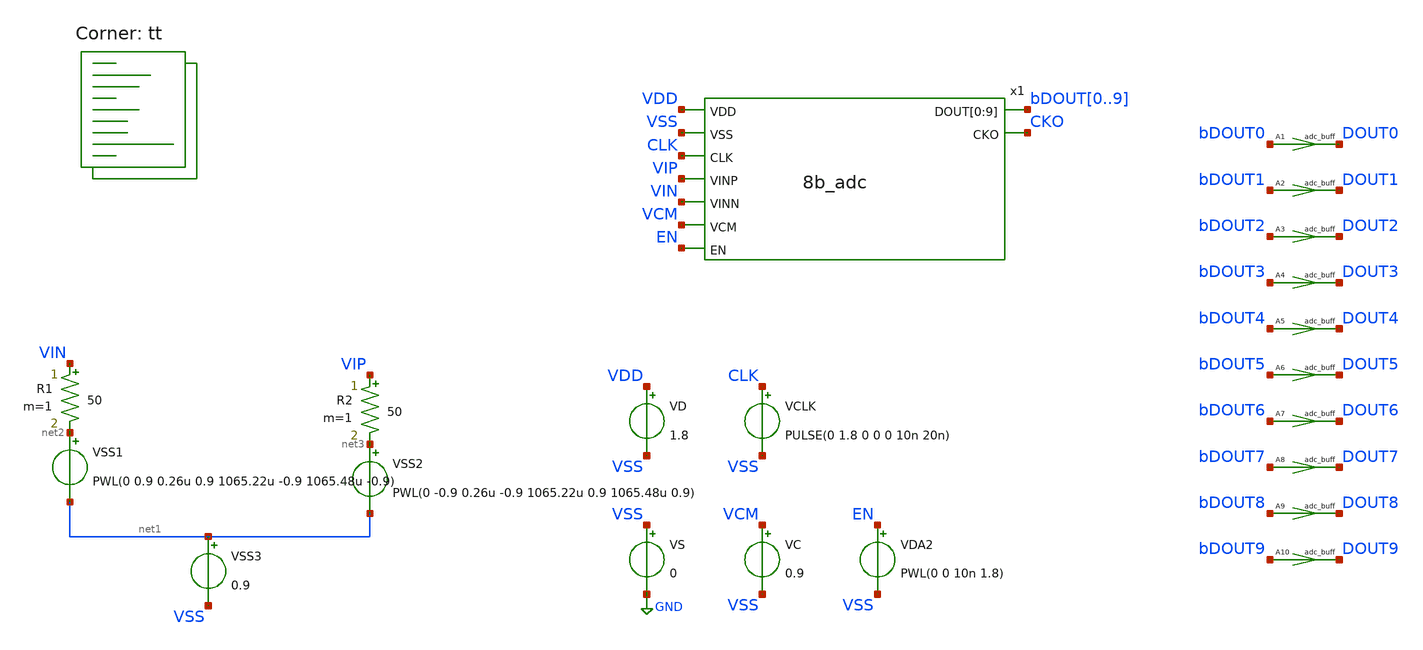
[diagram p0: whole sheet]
** sch_path: xschem/adc_tb_static.sch
**.subckt adc_tb_static
VSS1 net2 net1 PWL(0 0.9 0.26u 0.9 1065.22u -0.9 1065.48u -0.9)
VSS2 net3 net1 PWL(0 -0.9 0.26u -0.9 1065.22u 0.9 1065.48u 0.9)
VSS3 net1 VSS 0.9
R1 VIN net2 50 m=1
R2 VIP net3 50 m=1
VS VSS GND 0
VD VDD VSS 1.8
VCLK CLK VSS PULSE(0 1.8 0 0 0 10n 20n)
x1 VDD VSS CLK VIP VIN VCM EN bDOUT0 bDOUT1 bDOUT2 bDOUT3 bDOUT4 bDOUT5 bDOUT6 bDOUT7 bDOUT8 bDOUT9
+ CKO 8b_adc
VC VCM VSS 0.9
VDA2 EN VSS PWL(0 0 10n 1.8)
A1 [ bDOUT0 ] [ DOUT0 ] adc_buff
A2 [ bDOUT1 ] [ DOUT1 ] adc_buff
A3 [ bDOUT2 ] [ DOUT2 ] adc_buff
A4 [ bDOUT3 ] [ DOUT3 ] adc_buff
A5 [ bDOUT4 ] [ DOUT4 ] adc_buff
A6 [ bDOUT5 ] [ DOUT5 ] adc_buff
A7 [ bDOUT6 ] [ DOUT6 ] adc_buff
A8 [ bDOUT7 ] [ DOUT7 ] adc_buff
A9 [ bDOUT8 ] [ DOUT8 ] adc_buff
A10 [ bDOUT9 ] [ DOUT9 ] adc_buff
**** begin user architecture code

** opencircuitdesign pdks install
* .lib $::SKYWATER_MODELS/sky130.lib.spice tt
*.include $PDK_ROOT/$PDK/libs.ref/sky130_fd_sc_hdll/spice/sky130_fd_sc_hdll.spice
.include $PDK_ROOT/$PDK/libs.ref/sky130_fd_sc_hs/spice/sky130_fd_sc_hs.spice
*.include $PDK_ROOT/$PDK/libs.ref/sky130_fd_sc_hd/spice/sky130_fd_sc_hd.spice



.option wnflag=0 bypass=1
.options method=trap rawfile=binary
.options solver=klu nomod
Eout out 0 VALUE = { ((V(dout0)*512 + V(dout1)*256 + V(dout2)*128 + V(dout3)*64 + V(dout4)*32 + V(dout5)*16 + V(dout6)*8 + V(dout7)*4 + V(dout8)*2 + V(dout9)*1)/3.3) - 512 }
Epow pow 0 VALUE = { V(vdd)*(-i(vd)) }
.model adc_buff adc_bridge(in_low=0.18 in_high=1.62 rise_delay=100p fall_delay=100p)
.control
global netlist_dir .
set num_threads=16
save cko out pow vip vin x1.vcp x1.vcn
tran 1n 1066u 0 ; Mengubah start time menjadi 10n
rusage traniter trantime
meas tran inst_pow MAX pow from=1n to=1066u
meas tran avg_pow  AVG pow from=1n to=1066u
remzerovec
write adc10b_tb_static.raw
wrdata adc10b_tb_static.txt out cko pow vip vin
quit 1
.endc


.lib $::SKYWATER_MODELS/sky130.lib.spice tt
**** end user architecture code
**.ends
.GLOBAL GND
.end
